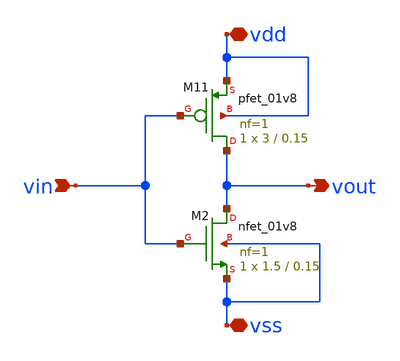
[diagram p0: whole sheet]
** sch_path: DIA2/inversor.sch
**.subckt inversor vin vout vdd vss
*.ipin vin
*.opin vout
*.iopin vdd
*.iopin vss
XM11 vout vin vdd vdd sky130_fd_pr__pfet_01v8 L=0.15 W=3 nf=1 ad='int((nf+1)/2) * W/nf * 0.29' as='int((nf+2)/2) * W/nf * 0.29'
+ pd='2*int((nf+1)/2) * (W/nf + 0.29)' ps='2*int((nf+2)/2) * (W/nf + 0.29)' nrd='0.29 / W' nrs='0.29 / W'
+ sa=0 sb=0 sd=0 mult=1 m=1
XM2 vout vin vss vss sky130_fd_pr__nfet_01v8 L=0.15 W=1.5 nf=1 ad='int((1 + 1)/2) * 1.5 / 1 * 0.29' as='int((1 + 2)/2) * 1.5 / 1 * 0.29'
+ pd='2*int((1 + 1)/2) * (1.5 / 1 + 0.29)' ps='2*int((1 + 2)/2) * (1.5 / 1 + 0.29)' nrd='0.29 / 1.5 ' nrs='0.29 / 1.5 '
+ sa=0 sb=0 sd=0 mult=1 m=1
**.ends
.end
